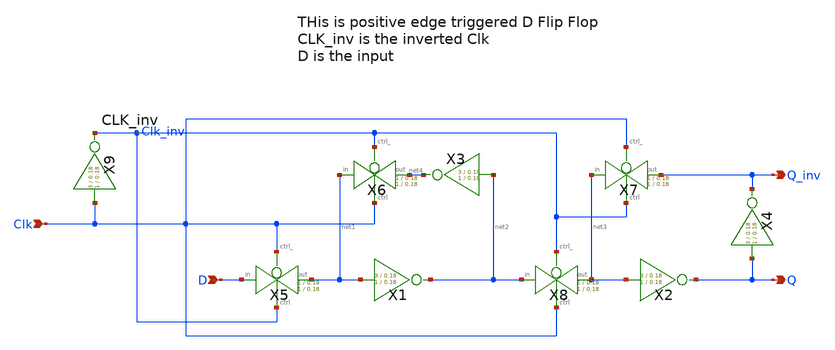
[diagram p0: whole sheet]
** sch_path: xschem/D_flip_flop/d_flip_flop.sch
**.subckt d_flip_flop D Clk Q_inv Q
*.ipin D
*.ipin Clk
*.opin Q_inv
*.opin Q
X1 net1 net2 inv Wpmos=3 Lpmos=0.18 Wnmos=1 Lnmos=0.18
X2 net3 Q inv Wpmos=3 Lpmos=0.18 Wnmos=1 Lnmos=0.18
X3 net2 net4 inv Wpmos=3 Lpmos=0.18 Wnmos=1 Lnmos=0.18
X4 Q Q_inv inv Wpmos=3 Lpmos=0.18 Wnmos=1 Lnmos=0.18
X5 D net1 Clk Clk_inv transmission_gate Wpmos=1 Lpmos=0.18 Wnmos=1 Lnmos=0.18
X6 net1 net4 Clk_inv Clk transmission_gate Wpmos=1 Lpmos=0.18 Wnmos=1 Lnmos=0.18
X7 net3 Q_inv Clk Clk_inv transmission_gate Wpmos=1 Lpmos=0.18 Wnmos=1 Lnmos=0.18
X8 net2 net3 Clk_inv Clk transmission_gate Wpmos=1 Lpmos=0.18 Wnmos=1 Lnmos=0.18
X9 Clk Clk_inv inv Wpmos=3 Lpmos=0.18 Wnmos=1 Lnmos=0.18
**.ends

* expanding   symbol:  inv/inv.sym # of pins=2
** sym_path: xschem/inv/inv.sym
** sch_path: xschem/inv/inv.sch
.subckt inv in out  Wpmos=3 Lpmos=0.18 Wnmos=1 Lnmos=0.18
*.ipin in
*.iopin out
XM1 out in GND GND sky130_fd_pr__nfet_01v8 L=Lnmos W=Wnmos nf=1 ad='int((nf+1)/2) * W/nf * 0.29' as='int((nf+2)/2) * W/nf * 0.29'
+ pd='2*int((nf+1)/2) * (W/nf + 0.29)' ps='2*int((nf+2)/2) * (W/nf + 0.29)' nrd='0.29 / W' nrs='0.29 / W'
+ sa=0 sb=0 sd=0 mult=1 m=1
XM2 out in VDD VDD sky130_fd_pr__pfet_01v8 L=Lpmos W=Wpmos nf=1 ad='int((nf+1)/2) * W/nf * 0.29' as='int((nf+2)/2) * W/nf * 0.29'
+ pd='2*int((nf+1)/2) * (W/nf + 0.29)' ps='2*int((nf+2)/2) * (W/nf + 0.29)' nrd='0.29 / W' nrs='0.29 / W'
+ sa=0 sb=0 sd=0 mult=1 m=1
.ends


* expanding   symbol:  transmission_gate/transmission_gate.sym # of pins=4
** sym_path: xschem/transmission_gate/transmission_gate.sym
** sch_path: xschem/transmission_gate/transmission_gate.sch
.subckt transmission_gate in out ctrl_ ctrl  Wpmos=1 Lpmos=0.18 Wnmos=1 Lnmos=0.18
*.iopin in
*.iopin out
*.ipin ctrl_
*.ipin ctrl
XM1 in ctrl out GND sky130_fd_pr__nfet_01v8 L=Lnmos W=Wnmos nf=1 ad='int((nf+1)/2) * W/nf * 0.29' as='int((nf+2)/2) * W/nf * 0.29'
+ pd='2*int((nf+1)/2) * (W/nf + 0.29)' ps='2*int((nf+2)/2) * (W/nf + 0.29)' nrd='0.29 / W' nrs='0.29 / W'
+ sa=0 sb=0 sd=0 mult=1 m=1
XM2 out ctrl_ in VDD sky130_fd_pr__pfet_01v8 L=Lpmos W=Wpmos nf=1 ad='int((nf+1)/2) * W/nf * 0.29' as='int((nf+2)/2) * W/nf * 0.29'
+ pd='2*int((nf+1)/2) * (W/nf + 0.29)' ps='2*int((nf+2)/2) * (W/nf + 0.29)' nrd='0.29 / W' nrs='0.29 / W'
+ sa=0 sb=0 sd=0 mult=1 m=1
.ends

.GLOBAL VDD
.GLOBAL GND
.end
